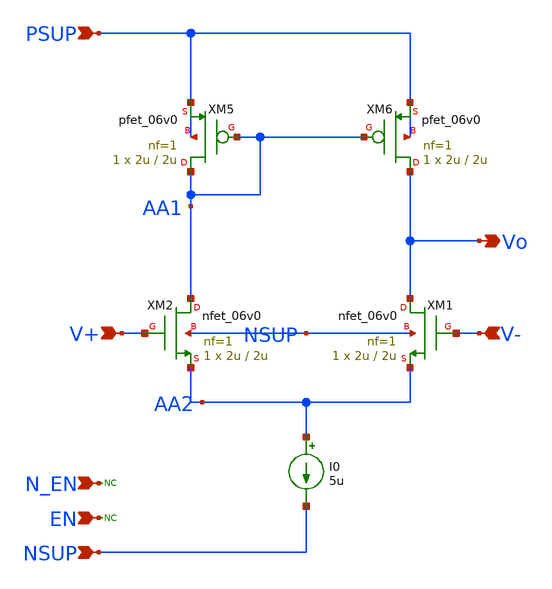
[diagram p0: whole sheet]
** sch_path: xschem/blocks/aux_amp/aux_amp.sch
**.subckt aux_amp PSUP NSUP N_EN EN V+ V- Vo
*.ipin PSUP
*.ipin NSUP
*.ipin N_EN
*.ipin EN
*.ipin V+
*.ipin V-
*.opin Vo
XM5 AA1 AA1 PSUP PSUP pfet_06v0 L=2u W=2u nf=1 ad='int((nf+1)/2) * W/nf * 0.18u' as='int((nf+2)/2) * W/nf * 0.18u'
+ pd='2*int((nf+1)/2) * (W/nf + 0.18u)' ps='2*int((nf+2)/2) * (W/nf + 0.18u)' nrd='0.18u / W' nrs='0.18u / W'
+ sa=0 sb=0 sd=0 m=1
XM6 Vo AA1 PSUP PSUP pfet_06v0 L=2u W=2u nf=1 ad='int((nf+1)/2) * W/nf * 0.18u' as='int((nf+2)/2) * W/nf * 0.18u'
+ pd='2*int((nf+1)/2) * (W/nf + 0.18u)' ps='2*int((nf+2)/2) * (W/nf + 0.18u)' nrd='0.18u / W' nrs='0.18u / W'
+ sa=0 sb=0 sd=0 m=1
I0 AA2 NSUP 5u
* noconn N_EN
* noconn EN
XM1 Vo V- AA2 NSUP nfet_06v0 L=2u W=2u nf=1 ad='int((nf+1)/2) * W/nf * 0.18u' as='int((nf+2)/2) * W/nf * 0.18u'
+ pd='2*int((nf+1)/2) * (W/nf + 0.18u)' ps='2*int((nf+2)/2) * (W/nf + 0.18u)' nrd='0.18u / W' nrs='0.18u / W'
+ sa=0 sb=0 sd=0 m=1
XM2 AA1 V+ AA2 NSUP nfet_06v0 L=2u W=2u nf=1 ad='int((nf+1)/2) * W/nf * 0.18u' as='int((nf+2)/2) * W/nf * 0.18u'
+ pd='2*int((nf+1)/2) * (W/nf + 0.18u)' ps='2*int((nf+2)/2) * (W/nf + 0.18u)' nrd='0.18u / W' nrs='0.18u / W'
+ sa=0 sb=0 sd=0 m=1
**.ends
.end
